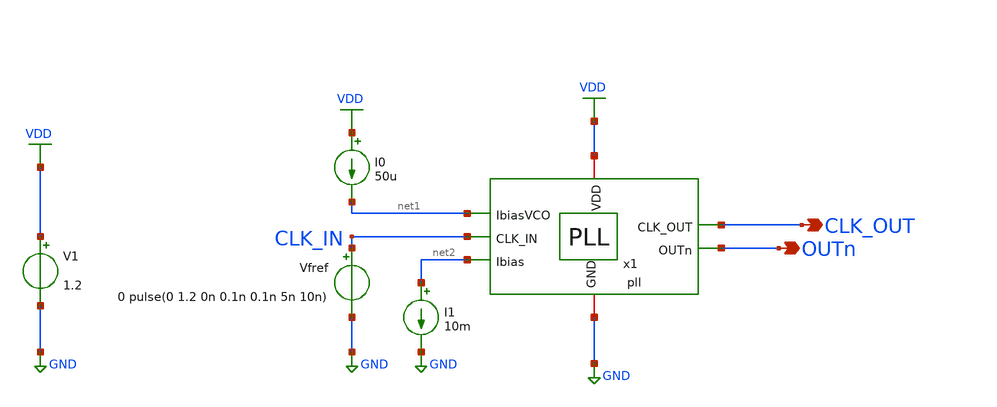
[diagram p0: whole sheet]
** sch_path: schematic/blocks/top-pll/top_pll_tb.sch
**.subckt top_pll_tb OUTn CLK_OUT
*.opin OUTn
*.opin CLK_OUT
V1 VDD GND 1.2
I0 VDD net1 50u
Vfref CLK_IN GND 0 pulse(0 1.2 0n 0.1n 0.1n 5n 10n)
I1 net2 GND 10m
x1 CLK_OUT CLK_IN net1 OUTn net2 VDD GND pll
**** begin user architecture code



.lib cornerMOSlv.lib mos_tt
.lib cornerHBT.lib hbt_typ
.lib cornerRES.lib res_typ
.lib cornerCAP.lib cap_typ_stat
.include /foss/pdks/ihp-sg13g2/libs.ref/sg13g2_stdcell/spice/sg13g2_stdcell.spice
.global VDD GND


.param CP_N_L = 0.5u
.param CP_N_W = 10u
.param CP_P_M = 1
.param CP_P_L = 0.5u
.param CP_P_W = 30u
.param CP_N_M = 1
.param C_CP = 400p






*****************************************************
* PLL + DSM Frequency Divider Testbench
*****************************************************

.option temp = 27
.param VDD = 1.2

* ==============================
* Include Models
* ==============================

* Inductor / analog models
.include ./IHP_4nH_Inductor.spice

.control
  *save all
  save x1.up x1.en x1.sdata x1.rst x1.sclk x1.dn x1.vctrl x1.clk_in x1.clk_out x1.dsm_out clk_in
+ clk_out outn
  * Simulation accuracy options
  .options maxstep=10p reltol=1e-4 abstol=1e-9

 * Run long enough for PLL lock
  tran 20p 5u uic
  remzerovec
  write pll_top.raw
.endc
* to generate following file copy stimuli.test
* to the simulation directory and run simulation -> Utile Stimuli Editor (GUI),
* and press 'Translate'
.include stimuli_test.cir





.meas tran tperiod_in TRIG v(clk_in) VAL=0.6 FALL=1 TARG v(clk_in) VAL=0.6 FALL=2
.meas tran ref_freq PARAM = '1e-6/tperiod_in'

.meas tran tperiod_out TRIG v(clk_out) VAL=0.6 FALL=1 TARG v(clk_out) VAL=0.6 FALL=2
.meas tran pll_freq PARAM = '1e-6/tperiod_out'


**** end user architecture code
**.ends
.GLOBAL GND
.GLOBAL VDD
.end
